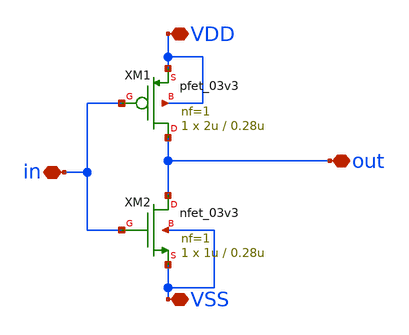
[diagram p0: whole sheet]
** sch_path: designs/digital/schematic/inv.sch
**.subckt inv VDD VSS in out
*.iopin VDD
*.iopin VSS
*.iopin in
*.iopin out
XM1 out in VDD VDD pfet_03v3 L=0.28u W=2u nf=1 ad='int((nf+1)/2) * W/nf * 0.18u' as='int((nf+2)/2) * W/nf * 0.18u'
+ pd='2*int((nf+1)/2) * (W/nf + 0.18u)' ps='2*int((nf+2)/2) * (W/nf + 0.18u)' nrd='0.18u / W' nrs='0.18u / W'
+ sa=0 sb=0 sd=0 m=1
XM2 out in VSS VSS nfet_03v3 L=0.28u W=1u nf=1 ad='int((nf+1)/2) * W/nf * 0.18u' as='int((nf+2)/2) * W/nf * 0.18u'
+ pd='2*int((nf+1)/2) * (W/nf + 0.18u)' ps='2*int((nf+2)/2) * (W/nf + 0.18u)' nrd='0.18u / W' nrs='0.18u / W'
+ sa=0 sb=0 sd=0 m=1
**.ends
.end
